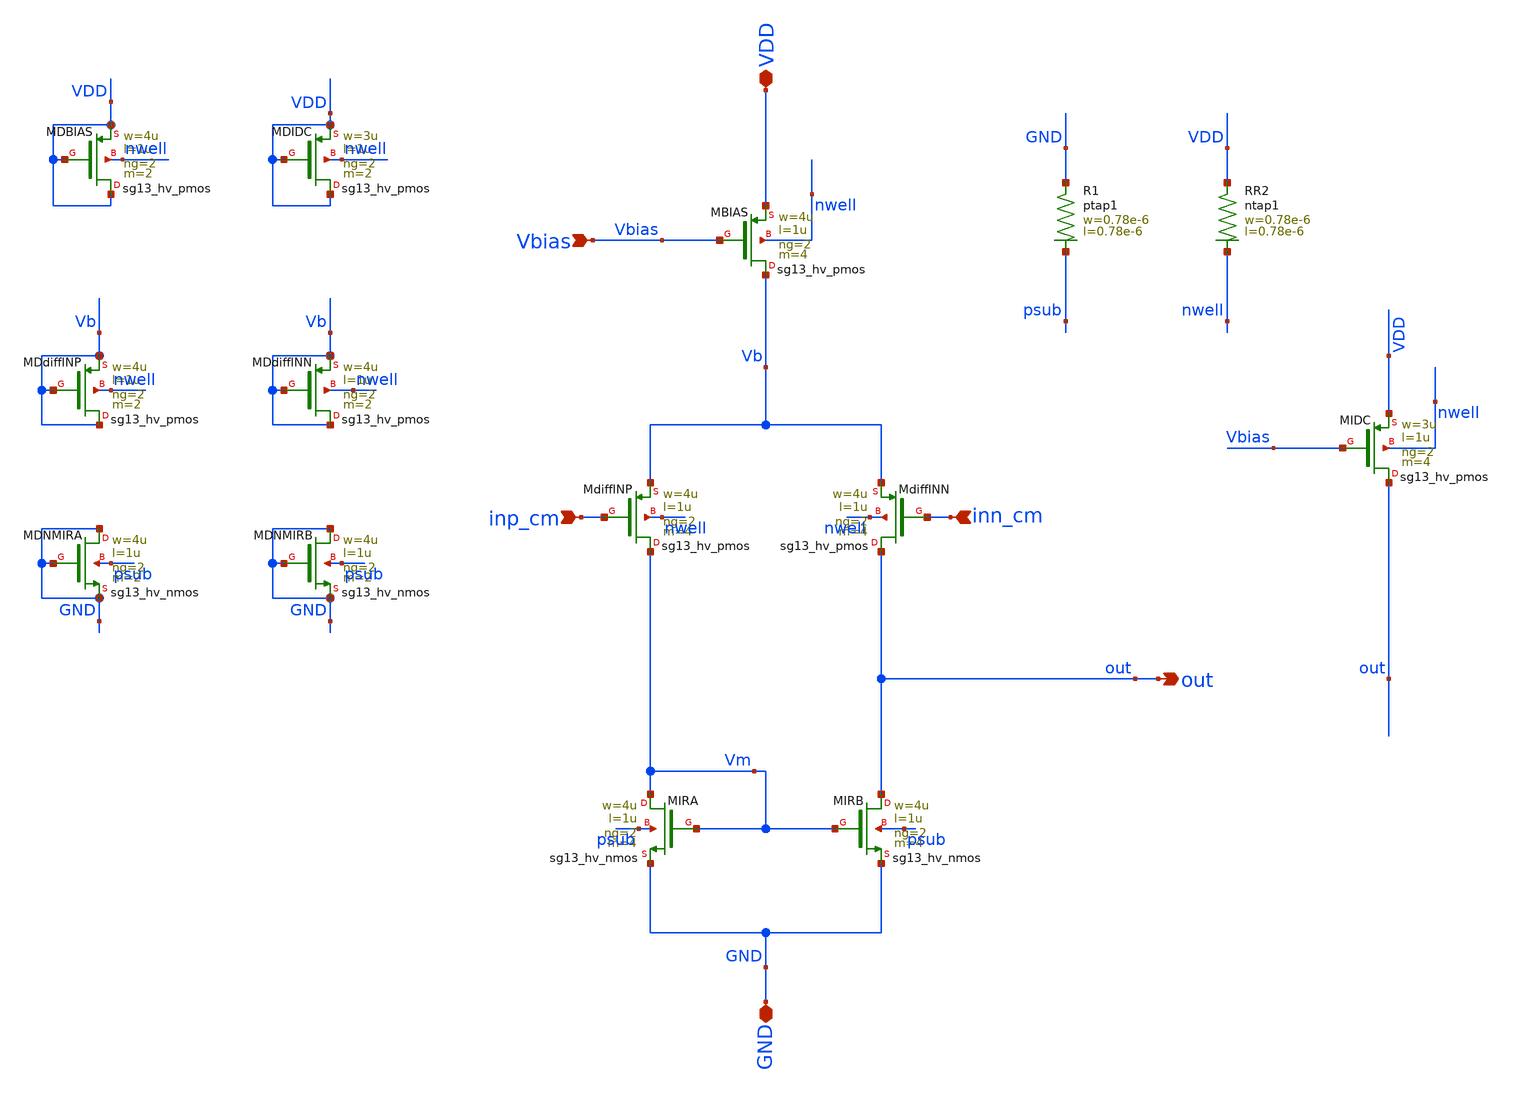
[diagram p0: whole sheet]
** sch_path: xschem/V2I_shift_final.sch
**.subckt V2I_shift_final inn_cm inp_cm out Vbias VDD GND
*.ipin inn_cm
*.ipin inp_cm
*.opin out
*.ipin Vbias
*.iopin VDD
*.iopin GND
XMIRA Vm Vm GND psub sg13_hv_nmos w=4u l=1u ng=2 m=4 mm_ok=1
XMBIAS Vb Vbias VDD nwell sg13_hv_pmos w=4u l=1u ng=2 m=4 mm_ok=1
XMIRB out Vm GND psub sg13_hv_nmos w=4u l=1u ng=2 m=4 mm_ok=1
XMdiffINN out inn_cm Vb nwell sg13_hv_pmos w=4u l=1u ng=2 m=4 mm_ok=1
XR1 GND psub ptap1 R=262.8 w=0.78e-6 l=0.78e-6
XR2 VDD nwell ntap1 R=262.8 w=0.78e-6 l=0.78e-6
XMDBIAS VDD VDD VDD nwell sg13_hv_pmos w=4u l=1u ng=2 m=2 mm_ok=1
XMIDC out Vbias VDD nwell sg13_hv_pmos w=3u l=1u ng=2 m=4 mm_ok=1
XMDIDC VDD VDD VDD nwell sg13_hv_pmos w=3u l=1u ng=2 m=2 mm_ok=1
XMdiffINP Vm inp_cm Vb nwell sg13_hv_pmos w=4u l=1u ng=2 m=4 mm_ok=1
XMDdiffINP Vb Vb Vb nwell sg13_hv_pmos w=4u l=1u ng=2 m=2 mm_ok=1
XMDdiffINN Vb Vb Vb nwell sg13_hv_pmos w=4u l=1u ng=2 m=2 mm_ok=1
XMDNMIRA GND GND GND psub sg13_hv_nmos w=4u l=1u ng=2 m=2 mm_ok=1
XMDNMIRB GND GND GND psub sg13_hv_nmos w=4u l=1u ng=2 m=2 mm_ok=1
**.ends
.end
